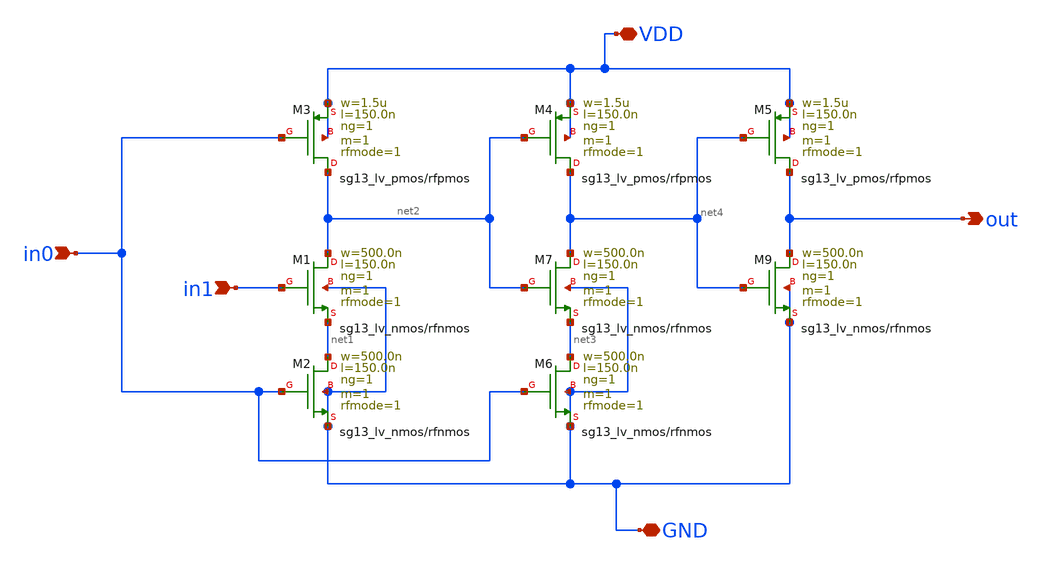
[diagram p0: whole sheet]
** sch_path: UWBPulseGenerator/design_data/xschem/phaseDetector.sch
**.subckt phaseDetector in0 in1 out GND VDD
*.ipin in0
*.ipin in1
*.opin out
*.iopin GND
*.iopin VDD
XM2 net1 in0 GND GND sg13_lv_nmos w=500.0n l=150.0n ng=1 m=1 rfmode=1 mm_ok=1
XM1 net2 in1 net1 GND sg13_lv_nmos w=500.0n l=150.0n ng=1 m=1 rfmode=1 mm_ok=1
XM3 net2 in0 VDD VDD sg13_lv_pmos w=1.5u l=150.0n ng=1 m=1 rfmode=1 mm_ok=1
XM4 net4 net2 VDD VDD sg13_lv_pmos w=1.5u l=150.0n ng=1 m=1 rfmode=1 mm_ok=1
XM5 out net4 VDD VDD sg13_lv_pmos w=1.5u l=150.0n ng=1 m=1 rfmode=1 mm_ok=1
XM6 net3 in0 GND GND sg13_lv_nmos w=500.0n l=150.0n ng=1 m=1 rfmode=1 mm_ok=1
XM7 net4 net2 net3 GND sg13_lv_nmos w=500.0n l=150.0n ng=1 m=1 rfmode=1 mm_ok=1
XM9 out net4 GND GND sg13_lv_nmos w=500.0n l=150.0n ng=1 m=1 rfmode=1 mm_ok=1
**.ends
.end
